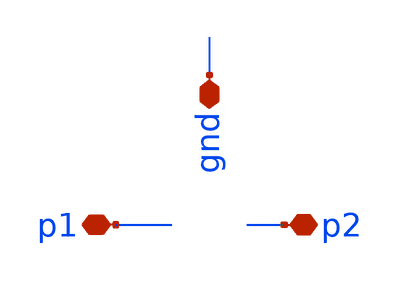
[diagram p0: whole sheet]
** sch_path: examples/sq_1nH_2.5GHz/xschem/lc-pex.sch
**.subckt lc-pex p1 p2 gnd
*.iopin p1
*.iopin p2
*.iopin gnd
**** begin user architecture code


* NGSPICE file created from lc-pex.ext - technology: sky130A

*.subckt lc-pex p1 p2 gnd
X0 p1.t0 p2.t3 sky130_fd_pr__cap_mim_m3_2 l=22.3 w=22.3
X1 p1.t1 p2.t2 sky130_fd_pr__cap_mim_m3_2 l=22.3 w=22.3
X2 p1.t2 p2.t1 sky130_fd_pr__cap_mim_m3_2 l=22.3 w=22.3
X3 p1.t3 p2.t0 sky130_fd_pr__cap_mim_m3_2 l=22.3 w=22.3
R0 p1.n2 p1.n0 0.348247
R1 p1.n1 p1.t3 0.0780897
R2 p1 p1.n2 0.070689
R3 p1.n0 p1.t1 0.0686501
R4 p1.n2 p1.n1 0.0520717
R5 p1.n0 p1.t2 0.000500104
R6 p1.n1 p1.t0 0.000500104
R7 p2.n0 p2.t3 0.495841
R8 p2.n1 p2.t1 0.49576
R9 p2 p2.n2 0.483229
R10 p2.n2 p2.n1 0.270536
R11 p2.n2 p2.n0 0.144491
R12 p2.n1 p2.t2 0.000906926
R13 p2.n0 p2.t0 0.000825541
C0 p1 p2 0.159p
*.ends



**** end user architecture code
**.ends
.end
